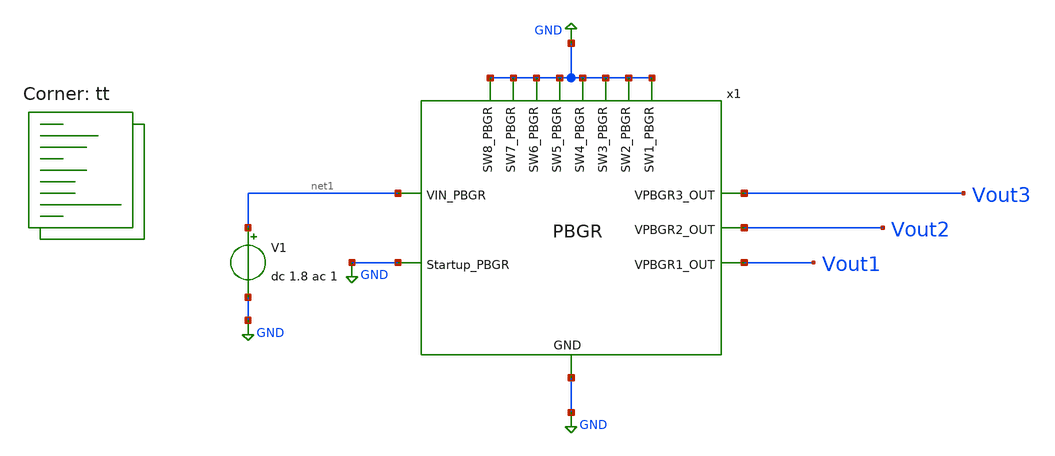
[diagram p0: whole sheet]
** sch_path: PBGR/Schematic Files/tb-try1.sch
**.subckt tb-try1
x1 net1 GND Vout3 Vout1 Vout2 GND GND GND GND GND GND GND GND GND PBGR
V1 net1 GND dc 1.8 ac 1
**** begin user architecture code
.lib $::SKYWATER_MODELS/sky130.lib.spice tt


.option wnflag=1
.option savecurrents
.temp 27
.control
save all
write tb-try1.raw
set appendwrite
op
write tb-try1.raw
**dc temp -50 150 1
ac dec 20 1 1e8
**plot v(Vout1) v(Vout2) v(Vout3)
**plot v(Vout1)
**plot v(Vout2)
**plot v(Vout3)
plot vdb(Vout1) vdb(Vout2) vdb(Vout3)
.endc


**** end user architecture code
**.ends
.GLOBAL GND
.end
